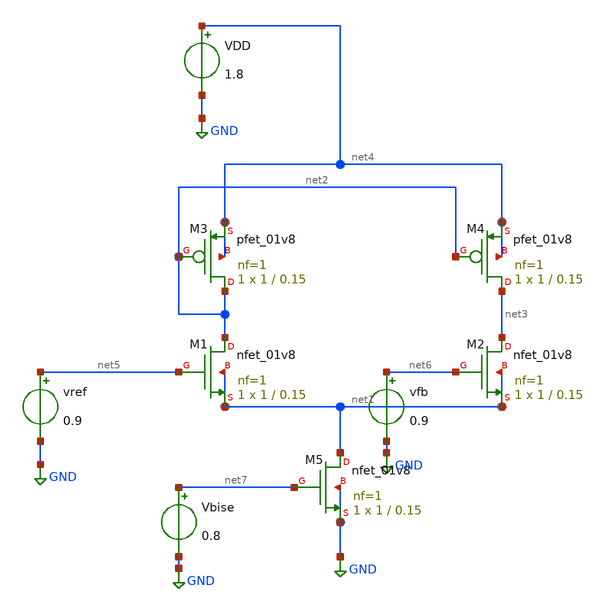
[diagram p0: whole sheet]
** sch_path: sky130/schematic/ota.sch
**.subckt ota
XM1 net2 net5 net1 net1 sky130_fd_pr__nfet_01v8 L=0.15 W=1 nf=1 ad='int((1 + 1)/2) * 1 / 1 * 0.29' as='int((1 + 2)/2) * 1 / 1 * 0.29'
+ pd='2*int((1 + 1)/2) * (1 / 1 + 0.29)' ps='2*int((1 + 2)/2) * (1 / 1 + 0.29)' nrd='0.29 / 1 ' nrs='0.29 / 1 '
+ sa=0 sb=0 sd=0 mult=1 m=1
XM2 net3 net6 net1 net1 sky130_fd_pr__nfet_01v8 L=0.15 W=1 nf=1 ad='int((1 + 1)/2) * 1 / 1 * 0.29' as='int((1 + 2)/2) * 1 / 1 * 0.29'
+ pd='2*int((1 + 1)/2) * (1 / 1 + 0.29)' ps='2*int((1 + 2)/2) * (1 / 1 + 0.29)' nrd='0.29 / 1 ' nrs='0.29 / 1 '
+ sa=0 sb=0 sd=0 mult=1 m=1
XM3 net2 net2 net4 net4 sky130_fd_pr__pfet_01v8 L=0.15 W=1 nf=1 ad='int((1 + 1)/2) * 1 / 1 * 0.29' as='int((1 + 2)/2) * 1 / 1 * 0.29'
+ pd='2*int((1 + 1)/2) * (1 / 1 + 0.29)' ps='2*int((1 + 2)/2) * (1 / 1 + 0.29)' nrd='0.29 / 1 ' nrs='0.29 / 1 '
+ sa=0 sb=0 sd=0 mult=1 m=1
XM4 net3 net2 net4 net4 sky130_fd_pr__pfet_01v8 L=0.15 W=1 nf=1 ad='int((1 + 1)/2) * 1 / 1 * 0.29' as='int((1 + 2)/2) * 1 / 1 * 0.29'
+ pd='2*int((1 + 1)/2) * (1 / 1 + 0.29)' ps='2*int((1 + 2)/2) * (1 / 1 + 0.29)' nrd='0.29 / 1 ' nrs='0.29 / 1 '
+ sa=0 sb=0 sd=0 mult=1 m=1
XM5 net1 net7 GND GND sky130_fd_pr__nfet_01v8 L=0.15 W=1 nf=1 ad='int((1 + 1)/2) * 1 / 1 * 0.29' as='int((1 + 2)/2) * 1 / 1 * 0.29'
+ pd='2*int((1 + 1)/2) * (1 / 1 + 0.29)' ps='2*int((1 + 2)/2) * (1 / 1 + 0.29)' nrd='0.29 / 1 ' nrs='0.29 / 1 '
+ sa=0 sb=0 sd=0 mult=1 m=1
VDD net4 GND 1.8
vref net5 GND 0.9
vfb net6 GND 0.9
Vbise net7 GND 0.8
**.ends
.GLOBAL GND
.end
